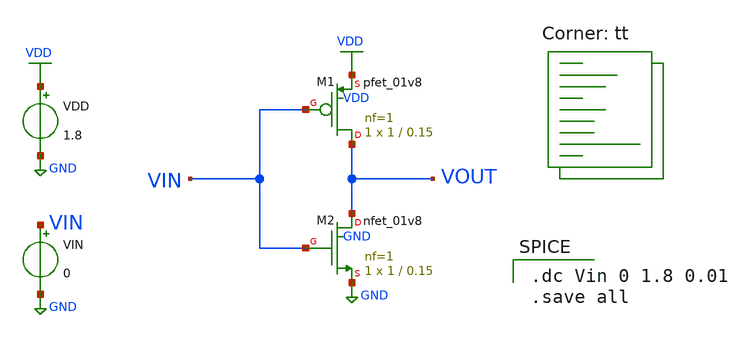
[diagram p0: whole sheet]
** sch_path: Design files/inverter1.sch
**.subckt inverter1
XM2 VOUT VIN GND GND sky130_fd_pr__nfet_01v8 L=0.15 W=1 nf=1 ad='int((1 + 1)/2) * 1 / 1 * 0.29' as='int((1 + 2)/2) * 1 / 1 * 0.29'
+ pd='2*int((1 + 1)/2) * (1 / 1 + 0.29)' ps='2*int((1 + 2)/2) * (1 / 1 + 0.29)' nrd='0.29 / 1 ' nrs='0.29 / 1 '
+ sa=0 sb=0 sd=0 mult=1 m=1
XM1 VOUT VIN VDD VDD sky130_fd_pr__pfet_01v8 L=0.15 W=1 nf=1 ad='int((1 + 1)/2) * 1 / 1 * 0.29' as='int((1 + 2)/2) * 1 / 1 * 0.29'
+ pd='2*int((1 + 1)/2) * (1 / 1 + 0.29)' ps='2*int((1 + 2)/2) * (1 / 1 + 0.29)' nrd='0.29 / 1 ' nrs='0.29 / 1 '
+ sa=0 sb=0 sd=0 mult=1 m=1
VDD VDD GND 1.8
VIN VIN GND 0
**** begin user architecture code
.lib $::SKYWATER_MODELS/sky130.lib.spice tt

.dc Vin 0 1.8 0.01
.save all

**** end user architecture code
**.ends
.GLOBAL VDD
.GLOBAL GND
.end
